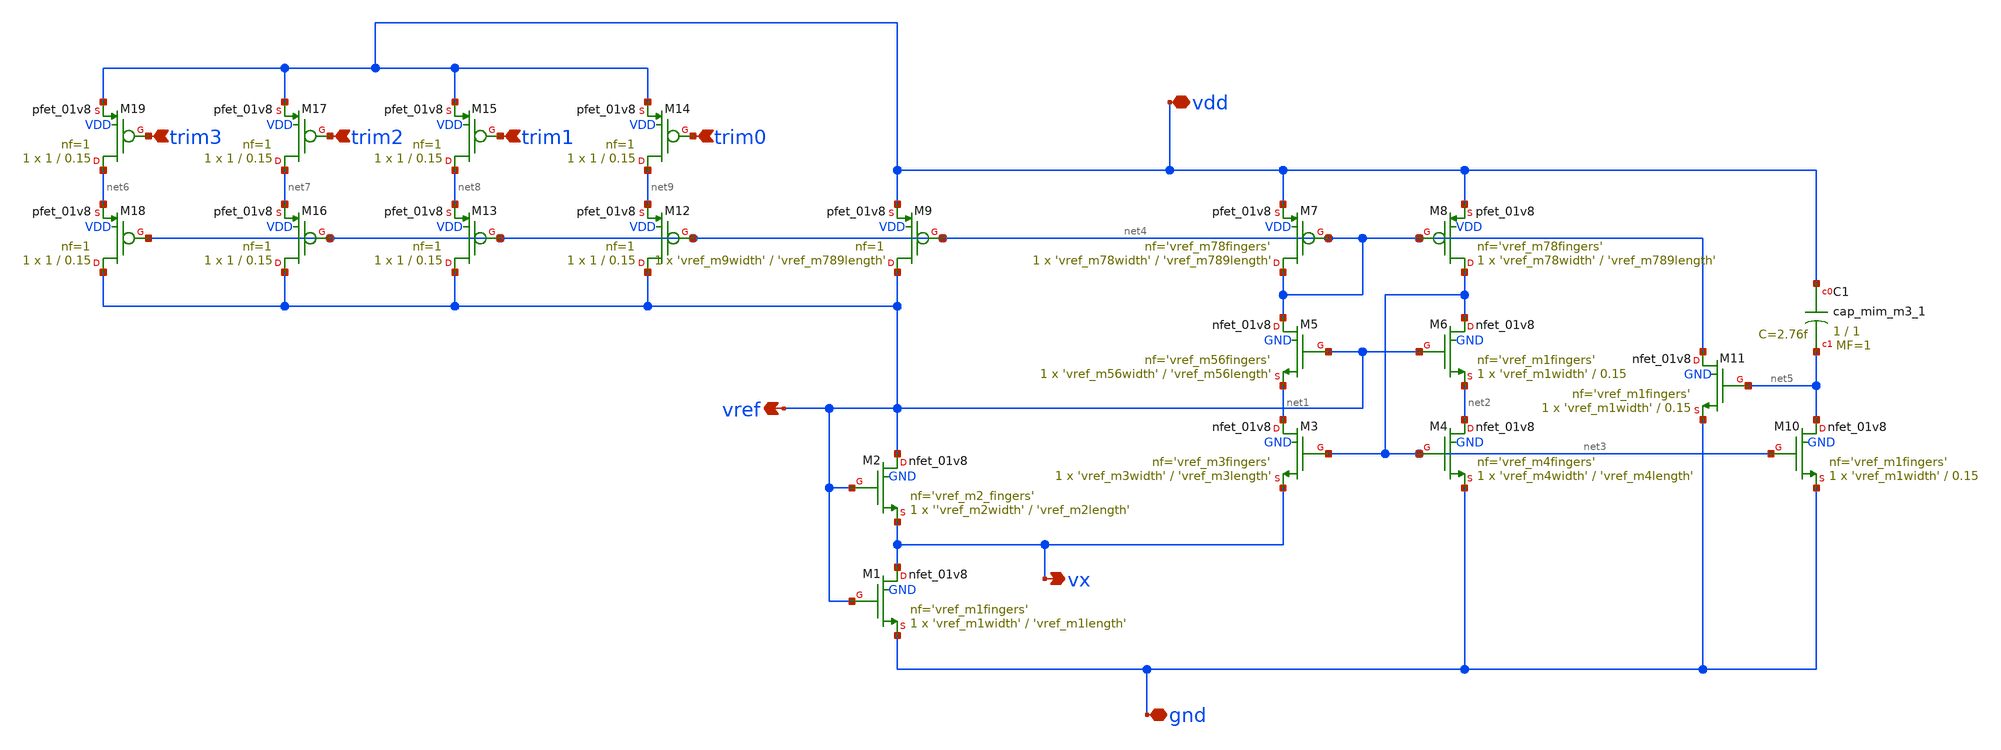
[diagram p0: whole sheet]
** sch_path: xschem/cmos_vref_param.sch
**.subckt cmos_vref_param vref gnd vdd vx trim0 trim1 trim2 trim3
*.opin vref
*.iopin gnd
*.iopin vdd
*.opin vx
*.ipin trim0
*.ipin trim1
*.ipin trim2
*.ipin trim3
XM2 vref vref vx GND sky130_fd_pr__nfet_01v8 L='vref_m2length' W=''vref_m2width' nf='vref_m2_fingers' ad='int((nf+1)/2)
+ * W/nf * 0.29' as='int((nf+2)/2) * W/nf * 0.29' pd='2*int((nf+1)/2) * (W/nf + 0.29)' ps='2*int((nf+2)/2)
+ * (W/nf + 0.29)' nrd='0.29 / W' nrs='0.29 / W' sa=0 sb=0 sd=0 mult=1 m=1
XM1 vx vref gnd GND sky130_fd_pr__nfet_01v8 L='vref_m1length' W='vref_m1width' nf='vref_m1fingers' ad='int((nf+1)/2)
+ * W/nf * 0.29' as='int((nf+2)/2) * W/nf * 0.29' pd='2*int((nf+1)/2) * (W/nf + 0.29)' ps='2*int((nf+2)/2)
+ * (W/nf + 0.29)' nrd='0.29 / W' nrs='0.29 / W' sa=0 sb=0 sd=0 mult=1 m=1
XM3 net1 net3 vx GND sky130_fd_pr__nfet_01v8 L='vref_m3length' W='vref_m3width' nf='vref_m3fingers' ad='int((nf+1)/2)
+ * W/nf * 0.29' as='int((nf+2)/2) * W/nf * 0.29' pd='2*int((nf+1)/2) * (W/nf + 0.29)' ps='2*int((nf+2)/2)
+ * (W/nf + 0.29)' nrd='0.29 / W' nrs='0.29 / W' sa=0 sb=0 sd=0 mult=1 m=1
XM4 net2 net3 gnd GND sky130_fd_pr__nfet_01v8 L='vref_m4length' W='vref_m4width' nf='vref_m4fingers' ad='int((nf+1)/2)
+ * W/nf * 0.29' as='int((nf+2)/2) * W/nf * 0.29' pd='2*int((nf+1)/2) * (W/nf + 0.29)' ps='2*int((nf+2)/2)
+ * (W/nf + 0.29)' nrd='0.29 / W' nrs='0.29 / W' sa=0 sb=0 sd=0 mult=1 m=1
XM5 net4 vref net1 GND sky130_fd_pr__nfet_01v8 L='vref_m56length' W='vref_m56width' nf='vref_m56fingers' ad='int((nf+1)/2)
+ * W/nf * 0.29' as='int((nf+2)/2) * W/nf * 0.29' pd='2*int((nf+1)/2) * (W/nf + 0.29)' ps='2*int((nf+2)/2)
+ * (W/nf + 0.29)' nrd='0.29 / W' nrs='0.29 / W' sa=0 sb=0 sd=0 mult=1 m=1
XM6 net3 vref net2 GND sky130_fd_pr__nfet_01v8 L=0.15 W='vref_m1width' nf='vref_m1fingers' ad='int((nf+1)/2)
+ * W/nf * 0.29' as='int((nf+2)/2) * W/nf * 0.29' pd='2*int((nf+1)/2) * (W/nf + 0.29)' ps='2*int((nf+2)/2)
+ * (W/nf + 0.29)' nrd='0.29 / W' nrs='0.29 / W' sa=0 sb=0 sd=0 mult=1 m=1
XM7 net4 net4 vdd VDD sky130_fd_pr__pfet_01v8 L='vref_m789length' W='vref_m78width' nf='vref_m78fingers' ad='int((nf+1)/2)
+ * W/nf * 0.29' as='int((nf+2)/2) * W/nf * 0.29' pd='2*int((nf+1)/2) * (W/nf + 0.29)' ps='2*int((nf+2)/2)
+ * (W/nf + 0.29)' nrd='0.29 / W' nrs='0.29 / W' sa=0 sb=0 sd=0 mult=1 m=1
XM8 net3 net4 vdd VDD sky130_fd_pr__pfet_01v8 L='vref_m789length' W='vref_m78width' nf='vref_m78fingers' ad='int((nf+1)/2)
+ * W/nf * 0.29' as='int((nf+2)/2) * W/nf * 0.29' pd='2*int((nf+1)/2) * (W/nf + 0.29)' ps='2*int((nf+2)/2)
+ * (W/nf + 0.29)' nrd='0.29 / W' nrs='0.29 / W' sa=0 sb=0 sd=0 mult=1 m=1
XM9 vref net4 vdd VDD sky130_fd_pr__pfet_01v8 L='vref_m789length' W='vref_m9width' nf=1 ad='int((nf+1)/2)
+ * W/nf * 0.29' as='int((nf+2)/2) * W/nf * 0.29' pd='2*int((nf+1)/2) * (W/nf + 0.29)' ps='2*int((nf+2)/2)
+ * (W/nf + 0.29)' nrd='0.29 / W' nrs='0.29 / W' sa=0 sb=0 sd=0 mult=1 m=1
XM10 net5 net3 gnd GND sky130_fd_pr__nfet_01v8 L=0.15 W='vref_m1width' nf='vref_m1fingers' ad='int((nf+1)/2)
+ * W/nf * 0.29' as='int((nf+2)/2) * W/nf * 0.29' pd='2*int((nf+1)/2) * (W/nf + 0.29)' ps='2*int((nf+2)/2)
+ * (W/nf + 0.29)' nrd='0.29 / W' nrs='0.29 / W' sa=0 sb=0 sd=0 mult=1 m=1
XM11 net4 net5 gnd GND sky130_fd_pr__nfet_01v8 L=0.15 W='vref_m1width' nf='vref_m1fingers' ad='int((nf+1)/2)
+ * W/nf * 0.29' as='int((nf+2)/2) * W/nf * 0.29' pd='2*int((nf+1)/2) * (W/nf + 0.29)' ps='2*int((nf+2)/2)
+ * (W/nf + 0.29)' nrd='0.29 / W' nrs='0.29 / W' sa=0 sb=0 sd=0 mult=1 m=1
XC1 vdd net5 sky130_fd_pr__cap_mim_m3_1 W=1 L=1 MF=1 m=1
XM12 vref net4 net9 VDD sky130_fd_pr__pfet_01v8 L=0.15 W=1 nf=1 ad='int((nf+1)/2) * W/nf * 0.29' as='int((nf+2)/2)
+ * W/nf * 0.29' pd='2*int((nf+1)/2) * (W/nf + 0.29)' ps='2*int((nf+2)/2) * (W/nf + 0.29)' nrd='0.29 /
+ W' nrs='0.29 / W' sa=0 sb=0 sd=0 mult=1 m=1
XM13 vref net4 net8 VDD sky130_fd_pr__pfet_01v8 L=0.15 W=1 nf=1 ad='int((nf+1)/2) * W/nf * 0.29' as='int((nf+2)/2)
+ * W/nf * 0.29' pd='2*int((nf+1)/2) * (W/nf + 0.29)' ps='2*int((nf+2)/2) * (W/nf + 0.29)' nrd='0.29 /
+ W' nrs='0.29 / W' sa=0 sb=0 sd=0 mult=1 m=1
XM14 net9 trim0 vdd VDD sky130_fd_pr__pfet_01v8 L=0.15 W=1 nf=1 ad='int((nf+1)/2) * W/nf * 0.29' as='int((nf+2)/2)
+ * W/nf * 0.29' pd='2*int((nf+1)/2) * (W/nf + 0.29)' ps='2*int((nf+2)/2) * (W/nf + 0.29)' nrd='0.29 /
+ W' nrs='0.29 / W' sa=0 sb=0 sd=0 mult=1 m=1
XM15 net8 trim1 vdd VDD sky130_fd_pr__pfet_01v8 L=0.15 W=1 nf=1 ad='int((nf+1)/2) * W/nf * 0.29' as='int((nf+2)/2)
+ * W/nf * 0.29' pd='2*int((nf+1)/2) * (W/nf + 0.29)' ps='2*int((nf+2)/2) * (W/nf + 0.29)' nrd='0.29 /
+ W' nrs='0.29 / W' sa=0 sb=0 sd=0 mult=1 m=1
XM16 vref net4 net7 VDD sky130_fd_pr__pfet_01v8 L=0.15 W=1 nf=1 ad='int((nf+1)/2) * W/nf * 0.29' as='int((nf+2)/2)
+ * W/nf * 0.29' pd='2*int((nf+1)/2) * (W/nf + 0.29)' ps='2*int((nf+2)/2) * (W/nf + 0.29)' nrd='0.29 /
+ W' nrs='0.29 / W' sa=0 sb=0 sd=0 mult=1 m=1
XM17 net7 trim2 vdd VDD sky130_fd_pr__pfet_01v8 L=0.15 W=1 nf=1 ad='int((nf+1)/2) * W/nf * 0.29' as='int((nf+2)/2)
+ * W/nf * 0.29' pd='2*int((nf+1)/2) * (W/nf + 0.29)' ps='2*int((nf+2)/2) * (W/nf + 0.29)' nrd='0.29 /
+ W' nrs='0.29 / W' sa=0 sb=0 sd=0 mult=1 m=1
XM18 vref net4 net6 VDD sky130_fd_pr__pfet_01v8 L=0.15 W=1 nf=1 ad='int((nf+1)/2) * W/nf * 0.29' as='int((nf+2)/2)
+ * W/nf * 0.29' pd='2*int((nf+1)/2) * (W/nf + 0.29)' ps='2*int((nf+2)/2) * (W/nf + 0.29)' nrd='0.29 /
+ W' nrs='0.29 / W' sa=0 sb=0 sd=0 mult=1 m=1
XM19 net6 trim3 vdd VDD sky130_fd_pr__pfet_01v8 L=0.15 W=1 nf=1 ad='int((nf+1)/2) * W/nf * 0.29' as='int((nf+2)/2)
+ * W/nf * 0.29' pd='2*int((nf+1)/2) * (W/nf + 0.29)' ps='2*int((nf+2)/2) * (W/nf + 0.29)' nrd='0.29 /
+ W' nrs='0.29 / W' sa=0 sb=0 sd=0 mult=1 m=1
**.ends
.end
